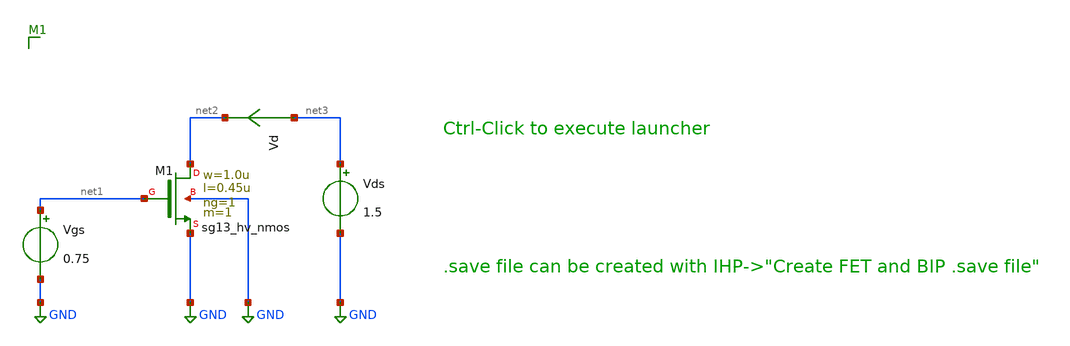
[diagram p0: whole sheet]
** sch_path: ihp-sg13g2/xschem_libs/sg13g2_tests_ase/dc_hv_nmos/schematic/dc_hv_nmos.sch
* Copyright 2023 IHP PDK Authors
**.subckt dc_hv_nmos
Vgs net1 GND 0.75
Vds net3 GND 1.5
Vd net3 net2 0
.save i(vd)
XM1 net2 net1 GND GND sg13_hv_nmos w=1.0u l=0.45u ng=1 m=1 mm_ok=1
**.ends
.GLOBAL GND
.end
